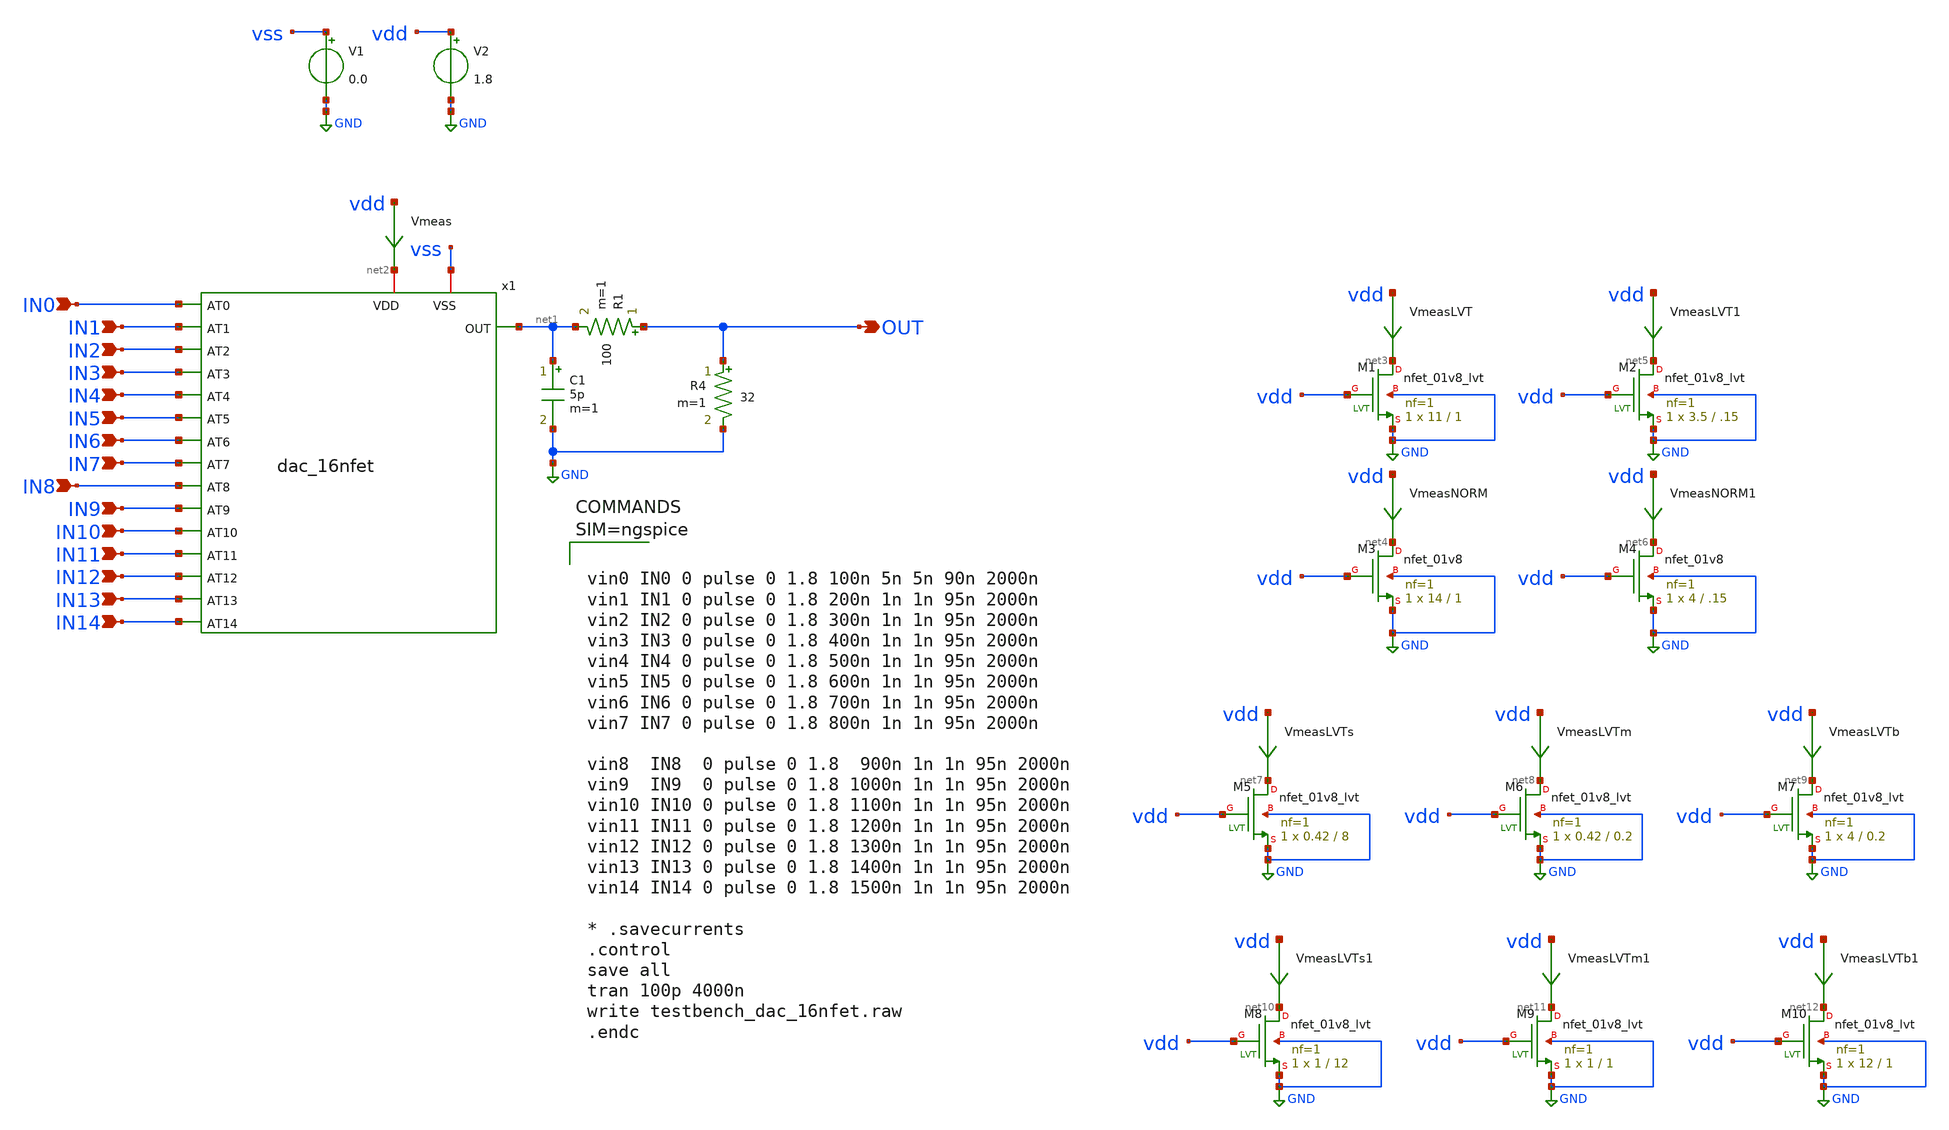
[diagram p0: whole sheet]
** sch_path: xschem/testbench_dac_16nfet.sch
**.subckt testbench_dac_16nfet IN1 OUT IN2 IN3 IN0 IN5 IN6 IN7 IN4 IN9 IN10 IN11 IN8 IN13 IN14 IN12
*.ipin IN1
*.opin OUT
*.ipin IN2
*.ipin IN3
*.ipin IN0
*.ipin IN5
*.ipin IN6
*.ipin IN7
*.ipin IN4
*.ipin IN9
*.ipin IN10
*.ipin IN11
*.ipin IN8
*.ipin IN13
*.ipin IN14
*.ipin IN12
x1 net2 IN0 IN1 IN2 IN3 IN4 IN5 IN6 IN7 IN8 IN9 IN10 IN11 IN12 IN13 IN14 net1 vss dac_16nfet
V1 vss GND 0.0
V2 vdd GND 1.8
R1 OUT net1 100 m=1
Vmeas vdd net2 0
.save i(vmeas)
R4 OUT GND 32 m=1
C1 net1 GND 5p m=1
XM1 net3 vdd GND GND sky130_fd_pr__nfet_01v8_lvt L=1 W=11 nf=1 ad='int((nf+1)/2) * W/nf * 0.29' as='int((nf+2)/2) * W/nf * 0.29'
+ pd='2*int((nf+1)/2) * (W/nf + 0.29)' ps='2*int((nf+2)/2) * (W/nf + 0.29)' nrd='0.29 / W' nrs='0.29 / W'
+ sa=0 sb=0 sd=0 mult=1 m=1
VmeasLVT vdd net3 0
.save i(vmeaslvt)
XM3 net4 vdd GND GND sky130_fd_pr__nfet_01v8 L=1 W=14 nf=1 ad='int((nf+1)/2) * W/nf * 0.29' as='int((nf+2)/2) * W/nf * 0.29'
+ pd='2*int((nf+1)/2) * (W/nf + 0.29)' ps='2*int((nf+2)/2) * (W/nf + 0.29)' nrd='0.29 / W' nrs='0.29 / W'
+ sa=0 sb=0 sd=0 mult=1 m=1
VmeasNORM vdd net4 0
.save i(vmeasnorm)
XM2 net5 vdd GND GND sky130_fd_pr__nfet_01v8_lvt L=.15 W=3.5 nf=1 ad='int((nf+1)/2) * W/nf * 0.29' as='int((nf+2)/2) * W/nf * 0.29'
+ pd='2*int((nf+1)/2) * (W/nf + 0.29)' ps='2*int((nf+2)/2) * (W/nf + 0.29)' nrd='0.29 / W' nrs='0.29 / W'
+ sa=0 sb=0 sd=0 mult=1 m=1
VmeasLVT1 vdd net5 0
.save i(vmeaslvt1)
XM4 net6 vdd GND GND sky130_fd_pr__nfet_01v8 L=.15 W=4 nf=1 ad='int((nf+1)/2) * W/nf * 0.29' as='int((nf+2)/2) * W/nf * 0.29'
+ pd='2*int((nf+1)/2) * (W/nf + 0.29)' ps='2*int((nf+2)/2) * (W/nf + 0.29)' nrd='0.29 / W' nrs='0.29 / W'
+ sa=0 sb=0 sd=0 mult=1 m=1
VmeasNORM1 vdd net6 0
.save i(vmeasnorm1)
XM5 net7 vdd GND GND sky130_fd_pr__nfet_01v8_lvt L=8 W=0.42 nf=1 ad='int((nf+1)/2) * W/nf * 0.29' as='int((nf+2)/2) * W/nf * 0.29'
+ pd='2*int((nf+1)/2) * (W/nf + 0.29)' ps='2*int((nf+2)/2) * (W/nf + 0.29)' nrd='0.29 / W' nrs='0.29 / W'
+ sa=0 sb=0 sd=0 mult=1 m=1
VmeasLVTs vdd net7 0
.save i(vmeaslvts)
XM6 net8 vdd GND GND sky130_fd_pr__nfet_01v8_lvt L=0.2 W=0.42 nf=1 ad='int((nf+1)/2) * W/nf * 0.29' as='int((nf+2)/2) * W/nf * 0.29'
+ pd='2*int((nf+1)/2) * (W/nf + 0.29)' ps='2*int((nf+2)/2) * (W/nf + 0.29)' nrd='0.29 / W' nrs='0.29 / W'
+ sa=0 sb=0 sd=0 mult=1 m=1
VmeasLVTm vdd net8 0
.save i(vmeaslvtm)
XM7 net9 vdd GND GND sky130_fd_pr__nfet_01v8_lvt L=0.2 W=4 nf=1 ad='int((nf+1)/2) * W/nf * 0.29' as='int((nf+2)/2) * W/nf * 0.29'
+ pd='2*int((nf+1)/2) * (W/nf + 0.29)' ps='2*int((nf+2)/2) * (W/nf + 0.29)' nrd='0.29 / W' nrs='0.29 / W'
+ sa=0 sb=0 sd=0 mult=1 m=1
VmeasLVTb vdd net9 0
.save i(vmeaslvtb)
XM8 net10 vdd GND GND sky130_fd_pr__nfet_01v8_lvt L=12 W=1 nf=1 ad='int((nf+1)/2) * W/nf * 0.29' as='int((nf+2)/2) * W/nf * 0.29'
+ pd='2*int((nf+1)/2) * (W/nf + 0.29)' ps='2*int((nf+2)/2) * (W/nf + 0.29)' nrd='0.29 / W' nrs='0.29 / W'
+ sa=0 sb=0 sd=0 mult=1 m=1
VmeasLVTs1 vdd net10 0
.save i(vmeaslvts1)
XM9 net11 vdd GND GND sky130_fd_pr__nfet_01v8_lvt L=1 W=1 nf=1 ad='int((nf+1)/2) * W/nf * 0.29' as='int((nf+2)/2) * W/nf * 0.29'
+ pd='2*int((nf+1)/2) * (W/nf + 0.29)' ps='2*int((nf+2)/2) * (W/nf + 0.29)' nrd='0.29 / W' nrs='0.29 / W'
+ sa=0 sb=0 sd=0 mult=1 m=1
VmeasLVTm1 vdd net11 0
.save i(vmeaslvtm1)
XM10 net12 vdd GND GND sky130_fd_pr__nfet_01v8_lvt L=1 W=12 nf=1 ad='int((nf+1)/2) * W/nf * 0.29' as='int((nf+2)/2) * W/nf * 0.29'
+ pd='2*int((nf+1)/2) * (W/nf + 0.29)' ps='2*int((nf+2)/2) * (W/nf + 0.29)' nrd='0.29 / W' nrs='0.29 / W'
+ sa=0 sb=0 sd=0 mult=1 m=1
VmeasLVTb1 vdd net12 0
.save i(vmeaslvtb1)
**** begin user architecture code

** opencircuitdesign pdks install
.lib $::SKYWATER_MODELS/sky130.lib.spice tt





vin0 IN0 0 pulse 0 1.8 100n 5n 5n 90n 2000n
vin1 IN1 0 pulse 0 1.8 200n 1n 1n 95n 2000n
vin2 IN2 0 pulse 0 1.8 300n 1n 1n 95n 2000n
vin3 IN3 0 pulse 0 1.8 400n 1n 1n 95n 2000n
vin4 IN4 0 pulse 0 1.8 500n 1n 1n 95n 2000n
vin5 IN5 0 pulse 0 1.8 600n 1n 1n 95n 2000n
vin6 IN6 0 pulse 0 1.8 700n 1n 1n 95n 2000n
vin7 IN7 0 pulse 0 1.8 800n 1n 1n 95n 2000n

vin8  IN8  0 pulse 0 1.8  900n 1n 1n 95n 2000n
vin9  IN9  0 pulse 0 1.8 1000n 1n 1n 95n 2000n
vin10 IN10 0 pulse 0 1.8 1100n 1n 1n 95n 2000n
vin11 IN11 0 pulse 0 1.8 1200n 1n 1n 95n 2000n
vin12 IN12 0 pulse 0 1.8 1300n 1n 1n 95n 2000n
vin13 IN13 0 pulse 0 1.8 1400n 1n 1n 95n 2000n
vin14 IN14 0 pulse 0 1.8 1500n 1n 1n 95n 2000n

* .savecurrents
.control
save all
tran 100p 4000n
write testbench_dac_16nfet.raw
.endc



**** end user architecture code
**.ends

* expanding   symbol:  dac_16nfet.sym # of pins=18
** sym_path: xschem/dac_16nfet.sym
** sch_path: xschem/dac_16nfet.sch
.subckt dac_16nfet VDD AT0 AT1 AT2 AT3 AT4 AT5 AT6 AT7 AT8 AT9 AT10 AT11 AT12 AT13 AT14 OUT VSS
*.ipin AT12
*.ipin AT13
*.iopin VDD
*.iopin VSS
*.opin OUT
*.ipin AT14
*.ipin AT4
*.ipin AT5
*.ipin AT6
*.ipin AT7
*.ipin AT8
*.ipin AT9
*.ipin AT10
*.ipin AT11
*.ipin AT0
*.ipin AT1
*.ipin AT2
*.ipin AT3
XM4 VDD AT0 OUT VSS sky130_fd_pr__nfet_01v8_lvt L=1 W=12 nf=1 ad='int((nf+1)/2) * W/nf * 0.29' as='int((nf+2)/2) * W/nf * 0.29'
+ pd='2*int((nf+1)/2) * (W/nf + 0.29)' ps='2*int((nf+2)/2) * (W/nf + 0.29)' nrd='0.29 / W' nrs='0.29 / W'
+ sa=0 sb=0 sd=0 mult=1 m=1
XM14 VDD AT1 OUT VSS sky130_fd_pr__nfet_01v8_lvt L=1 W=8.484 nf=1 ad='int((nf+1)/2) * W/nf * 0.29' as='int((nf+2)/2) * W/nf * 0.29'
+ pd='2*int((nf+1)/2) * (W/nf + 0.29)' ps='2*int((nf+2)/2) * (W/nf + 0.29)' nrd='0.29 / W' nrs='0.29 / W'
+ sa=0 sb=0 sd=0 mult=1 m=1
XM15 VDD AT2 OUT VSS sky130_fd_pr__nfet_01v8_lvt L=1 W=6 nf=1 ad='int((nf+1)/2) * W/nf * 0.29' as='int((nf+2)/2) * W/nf * 0.29'
+ pd='2*int((nf+1)/2) * (W/nf + 0.29)' ps='2*int((nf+2)/2) * (W/nf + 0.29)' nrd='0.29 / W' nrs='0.29 / W'
+ sa=0 sb=0 sd=0 mult=1 m=1
XM16 VDD AT3 OUT VSS sky130_fd_pr__nfet_01v8_lvt L=1 W=4.24 nf=1 ad='int((nf+1)/2) * W/nf * 0.29' as='int((nf+2)/2) * W/nf * 0.29'
+ pd='2*int((nf+1)/2) * (W/nf + 0.29)' ps='2*int((nf+2)/2) * (W/nf + 0.29)' nrd='0.29 / W' nrs='0.29 / W'
+ sa=0 sb=0 sd=0 mult=1 m=1
XM9 VDD AT4 OUT VSS sky130_fd_pr__nfet_01v8_lvt L=1 W=3 nf=1 ad='int((nf+1)/2) * W/nf * 0.29' as='int((nf+2)/2) * W/nf * 0.29'
+ pd='2*int((nf+1)/2) * (W/nf + 0.29)' ps='2*int((nf+2)/2) * (W/nf + 0.29)' nrd='0.29 / W' nrs='0.29 / W'
+ sa=0 sb=0 sd=0 mult=1 m=1
XM10 VDD AT5 OUT VSS sky130_fd_pr__nfet_01v8_lvt L=1 W=2.12 nf=1 ad='int((nf+1)/2) * W/nf * 0.29' as='int((nf+2)/2) * W/nf * 0.29'
+ pd='2*int((nf+1)/2) * (W/nf + 0.29)' ps='2*int((nf+2)/2) * (W/nf + 0.29)' nrd='0.29 / W' nrs='0.29 / W'
+ sa=0 sb=0 sd=0 mult=1 m=1
XM12 VDD AT7 OUT VSS sky130_fd_pr__nfet_01v8_lvt L=1 W=1 nf=1 ad='int((nf+1)/2) * W/nf * 0.29' as='int((nf+2)/2) * W/nf * 0.29'
+ pd='2*int((nf+1)/2) * (W/nf + 0.29)' ps='2*int((nf+2)/2) * (W/nf + 0.29)' nrd='0.29 / W' nrs='0.29 / W'
+ sa=0 sb=0 sd=0 mult=1 m=1
XM1 VDD AT14 OUT VSS sky130_fd_pr__nfet_01v8_lvt L=12 W=1 nf=1 ad='int((nf+1)/2) * W/nf * 0.29' as='int((nf+2)/2) * W/nf * 0.29'
+ pd='2*int((nf+1)/2) * (W/nf + 0.29)' ps='2*int((nf+2)/2) * (W/nf + 0.29)' nrd='0.29 / W' nrs='0.29 / W'
+ sa=0 sb=0 sd=0 mult=1 m=1
XM2 VDD AT13 OUT VSS sky130_fd_pr__nfet_01v8_lvt L=8.484 W=1 nf=1 ad='int((nf+1)/2) * W/nf * 0.29' as='int((nf+2)/2) * W/nf * 0.29'
+ pd='2*int((nf+1)/2) * (W/nf + 0.29)' ps='2*int((nf+2)/2) * (W/nf + 0.29)' nrd='0.29 / W' nrs='0.29 / W'
+ sa=0 sb=0 sd=0 mult=1 m=1
XM3 VDD AT12 OUT VSS sky130_fd_pr__nfet_01v8_lvt L=6 W=1 nf=1 ad='int((nf+1)/2) * W/nf * 0.29' as='int((nf+2)/2) * W/nf * 0.29'
+ pd='2*int((nf+1)/2) * (W/nf + 0.29)' ps='2*int((nf+2)/2) * (W/nf + 0.29)' nrd='0.29 / W' nrs='0.29 / W'
+ sa=0 sb=0 sd=0 mult=1 m=1
XM5 VDD AT11 OUT VSS sky130_fd_pr__nfet_01v8_lvt L=4.24 W=1 nf=1 ad='int((nf+1)/2) * W/nf * 0.29' as='int((nf+2)/2) * W/nf * 0.29'
+ pd='2*int((nf+1)/2) * (W/nf + 0.29)' ps='2*int((nf+2)/2) * (W/nf + 0.29)' nrd='0.29 / W' nrs='0.29 / W'
+ sa=0 sb=0 sd=0 mult=1 m=1
XM6 VDD AT10 OUT VSS sky130_fd_pr__nfet_01v8_lvt L=3 W=1 nf=1 ad='int((nf+1)/2) * W/nf * 0.29' as='int((nf+2)/2) * W/nf * 0.29'
+ pd='2*int((nf+1)/2) * (W/nf + 0.29)' ps='2*int((nf+2)/2) * (W/nf + 0.29)' nrd='0.29 / W' nrs='0.29 / W'
+ sa=0 sb=0 sd=0 mult=1 m=1
XM7 VDD AT9 OUT VSS sky130_fd_pr__nfet_01v8_lvt L=2.12 W=1 nf=1 ad='int((nf+1)/2) * W/nf * 0.29' as='int((nf+2)/2) * W/nf * 0.29'
+ pd='2*int((nf+1)/2) * (W/nf + 0.29)' ps='2*int((nf+2)/2) * (W/nf + 0.29)' nrd='0.29 / W' nrs='0.29 / W'
+ sa=0 sb=0 sd=0 mult=1 m=1
XM8 VDD AT6 OUT VSS sky130_fd_pr__nfet_01v8_lvt L=1 W=1.5 nf=1 ad='int((nf+1)/2) * W/nf * 0.29' as='int((nf+2)/2) * W/nf * 0.29'
+ pd='2*int((nf+1)/2) * (W/nf + 0.29)' ps='2*int((nf+2)/2) * (W/nf + 0.29)' nrd='0.29 / W' nrs='0.29 / W'
+ sa=0 sb=0 sd=0 mult=1 m=1
XM11 VDD AT8 OUT VSS sky130_fd_pr__nfet_01v8_lvt L=1.5 W=1 nf=1 ad='int((nf+1)/2) * W/nf * 0.29' as='int((nf+2)/2) * W/nf * 0.29'
+ pd='2*int((nf+1)/2) * (W/nf + 0.29)' ps='2*int((nf+2)/2) * (W/nf + 0.29)' nrd='0.29 / W' nrs='0.29 / W'
+ sa=0 sb=0 sd=0 mult=1 m=1
.ends

.GLOBAL GND
.end
